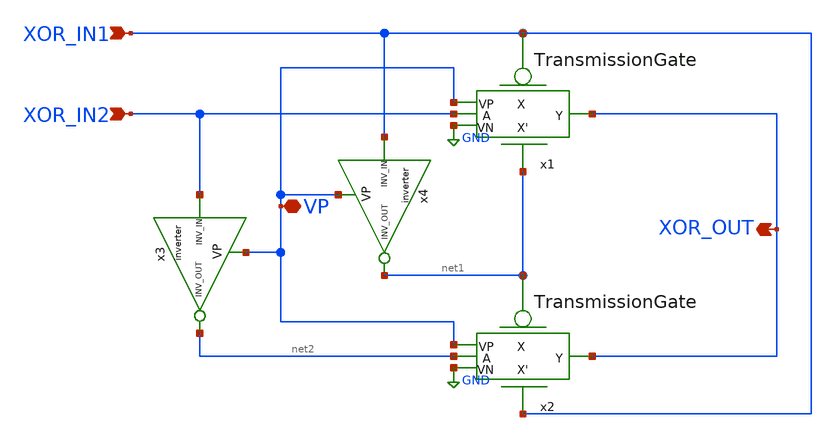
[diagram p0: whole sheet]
** sch_path: AllSymbols&Sch/Gates/XORTransmissonGate.sch
**.subckt XORTransmissonGate XOR_IN2 XOR_IN1 XOR_OUT VP
*.ipin XOR_IN2
*.ipin XOR_IN1
*.opin XOR_OUT
*.iopin VP
x1 XOR_IN1 VP XOR_IN2 XOR_OUT GND net1 TransmissionGate
x2 net1 VP net2 XOR_OUT GND XOR_IN1 TransmissionGate
x3 VP net2 XOR_IN2 inverter
x4 VP net1 XOR_IN1 inverter
**.ends

* expanding   symbol:
*+  /home/safal/projects/GitHub_CMOS_4bit_ALU/AllSymbols&Sch/GenericSym/TransmissionGate.sym # of pins=6
** sym_path: AllSymbols&Sch/GenericSym/TransmissionGate.sym
** sch_path: AllSymbols&Sch/GenericSym/TransmissionGate.sch
.subckt TransmissionGate X VP A Y VN X'
*.ipin A
*.opin Y
*.ipin X'
*.ipin X
*.iopin VP
*.iopin VN
XM1 A X Y VP sky130_fd_pr__pfet_01v8 L=0.15 W=1 nf=1 ad='int((1 + 1)/2) * 1 / 1 * 0.29' as='int((1 + 2)/2) * 1 / 1 * 0.29'
+ pd='2*int((1 + 1)/2) * (1 / 1 + 0.29)' ps='2*int((1 + 2)/2) * (1 / 1 + 0.29)' nrd='0.29 / 1 ' nrs='0.29 / 1 '
+ sa=0 sb=0 sd=0 mult=1 m=1
XM2 A X' Y VN sky130_fd_pr__nfet_01v8 L=0.15 W=1 nf=1 ad='int((1 + 1)/2) * 1 / 1 * 0.29' as='int((1 +
+ 2)/2) * 1 / 1 * 0.29' pd='2*int((1 + 1)/2) * (1 / 1 + 0.29)' ps='2*int((1 + 2)/2) * (1 / 1 + 0.29)' nrd='0.29
+ / 1 ' nrs='0.29 / 1 ' sa=0 sb=0 sd=0 mult=1 m=1
**** begin user architecture code

.lib /usr/local/share/pdk/sky130A/libs.tech/ngspice/sky130.lib.spice tt

**** end user architecture code
.ends


* expanding   symbol:  /home/safal/projects/GitHub_CMOS_4bit_ALU/AllSymbols&Sch/GenericSym/inverter.sym # of pins=3
** sym_path: AllSymbols&Sch/GenericSym/inverter.sym
** sch_path: AllSymbols&Sch/GenericSym/inverter.sch
.subckt inverter VP inv_out inv_in
*.ipin inv_in
*.opin inv_out
*.iopin VP
XM1 inv_out inv_in VP VP sky130_fd_pr__pfet_01v8 L=0.15 W=2 nf=1 ad='int((1 + 1)/2) * 2 / 1 * 0.29' as='int((1
+ + 2)/2) * 2 / 1 * 0.29' pd='2*int((1 + 1)/2) * (2 / 1 + 0.29)' ps='2*int((1 + 2)/2) * (2 / 1 + 0.29)' nrd='0.29
+ / 2 ' nrs='0.29 / 2 ' sa=0 sb=0 sd=0 mult=1 m=1
XM2 inv_out inv_in GND GND sky130_fd_pr__nfet_01v8 L=0.15 W=1 nf=1 ad='int((1 + 1)/2) * 1 / 1 * 0.29' as='int((1
+ + 2)/2) * 1 / 1 * 0.29' pd='2*int((1 + 1)/2) * (1 / 1 + 0.29)' ps='2*int((1 + 2)/2) * (1 / 1 + 0.29)' nrd='0.29
+ / 1 ' nrs='0.29 / 1 ' sa=0 sb=0 sd=0 mult=1 m=1
.ends

.GLOBAL GND
.end
